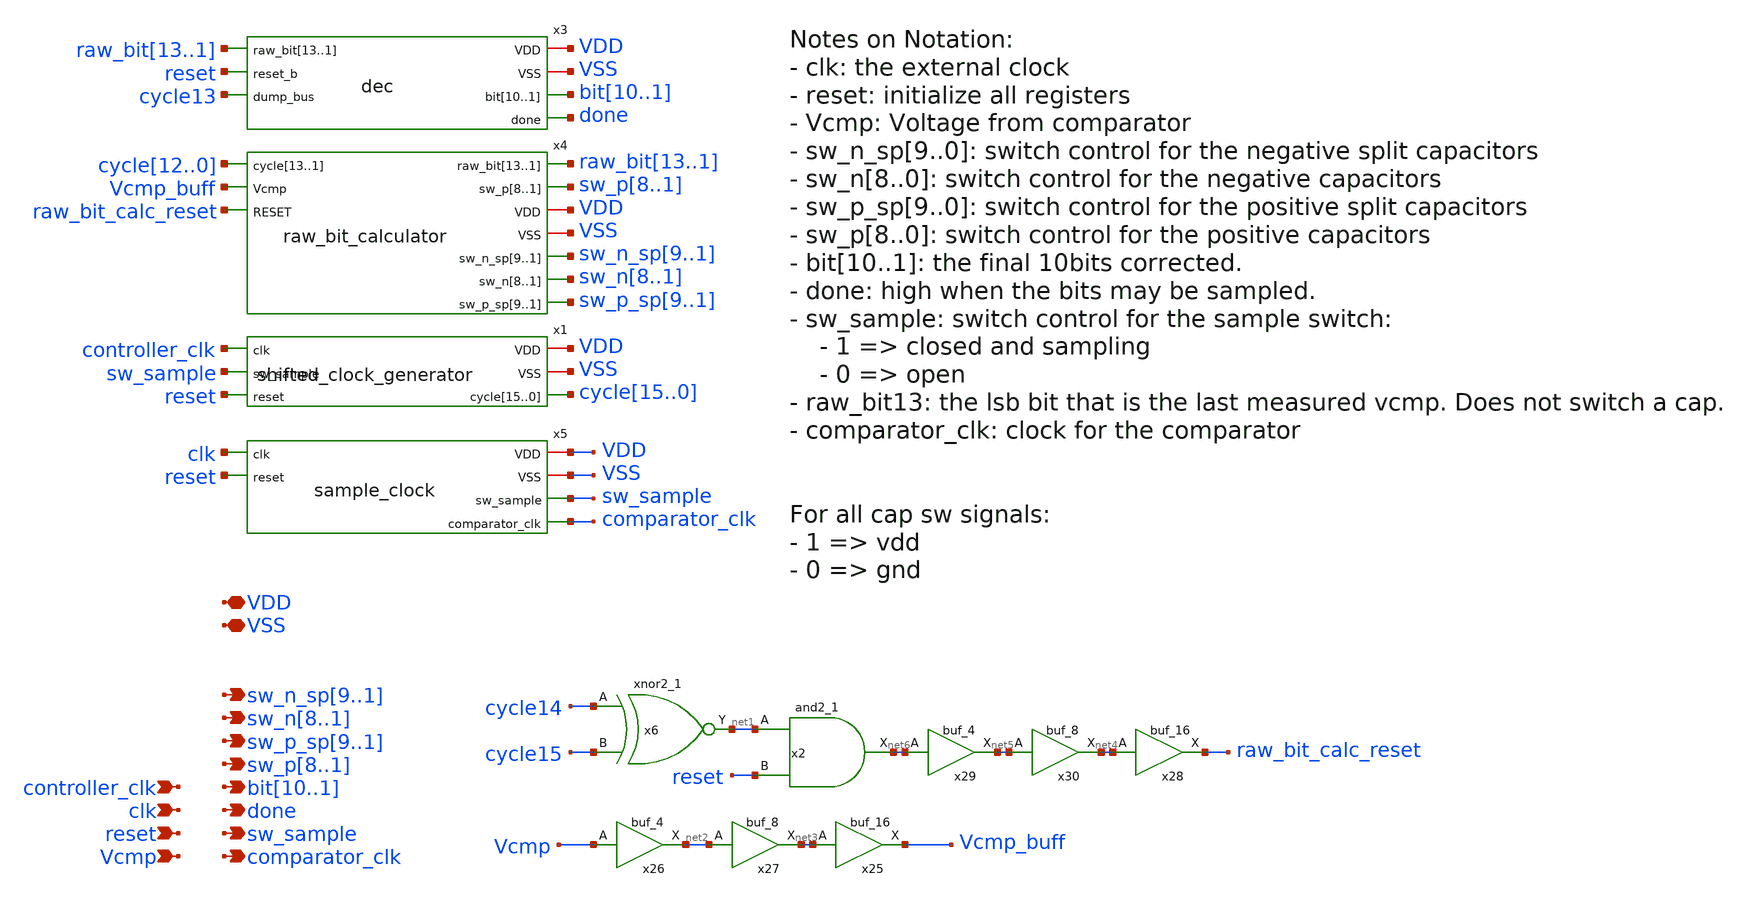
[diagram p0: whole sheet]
** sch_path: xschem/src/controller/controller.sch
**.subckt controller clk
*+ sw_n_sp9,sw_n_sp8,sw_n_sp7,sw_n_sp6,sw_n_sp5,sw_n_sp4,sw_n_sp3,sw_n_sp2,sw_n_sp1 VSS VDD reset Vcmp sw_n8,sw_n7,sw_n6,sw_n5,sw_n4,sw_n3,sw_n2,sw_n1
*+ sw_p_sp9,sw_p_sp8,sw_p_sp7,sw_p_sp6,sw_p_sp5,sw_p_sp4,sw_p_sp3,sw_p_sp2,sw_p_sp1 sw_p8,sw_p7,sw_p6,sw_p5,sw_p4,sw_p3,sw_p2,sw_p1 bit10,bit9,bit8,bit7,bit6,bit5,bit4,bit3,bit2,bit1
*+ done sw_sample controller_clk comparator_clk
*.ipin clk
*.opin sw_n_sp9,sw_n_sp8,sw_n_sp7,sw_n_sp6,sw_n_sp5,sw_n_sp4,sw_n_sp3,sw_n_sp2,sw_n_sp1
*.iopin VSS
*.iopin VDD
*.ipin reset
*.ipin Vcmp
*.opin sw_n8,sw_n7,sw_n6,sw_n5,sw_n4,sw_n3,sw_n2,sw_n1
*.opin sw_p_sp9,sw_p_sp8,sw_p_sp7,sw_p_sp6,sw_p_sp5,sw_p_sp4,sw_p_sp3,sw_p_sp2,sw_p_sp1
*.opin sw_p8,sw_p7,sw_p6,sw_p5,sw_p4,sw_p3,sw_p2,sw_p1
*.opin bit10,bit9,bit8,bit7,bit6,bit5,bit4,bit3,bit2,bit1
*.opin done
*.opin sw_sample
*.ipin controller_clk
*.opin comparator_clk
x3 VDD raw_bit13 raw_bit12 raw_bit11 raw_bit10 raw_bit9 raw_bit8 raw_bit7 raw_bit6 raw_bit5 raw_bit4
+ raw_bit3 raw_bit2 raw_bit1 VSS reset bit10 bit9 bit8 bit7 bit6 bit5 bit4 bit3 bit2 bit1 done cycle13 dec
x4 raw_bit13 raw_bit12 raw_bit11 raw_bit10 raw_bit9 raw_bit8 raw_bit7 raw_bit6 raw_bit5 raw_bit4
+ raw_bit3 raw_bit2 raw_bit1 cycle12 cycle11 cycle10 cycle9 cycle8 cycle7 cycle6 cycle5 cycle4 cycle3 cycle2
+ cycle1 cycle0 sw_p8 sw_p7 sw_p6 sw_p5 sw_p4 sw_p3 sw_p2 sw_p1 Vcmp_buff raw_bit_calc_reset VDD VSS
+ sw_n_sp9 sw_n_sp8 sw_n_sp7 sw_n_sp6 sw_n_sp5 sw_n_sp4 sw_n_sp3 sw_n_sp2 sw_n_sp1 sw_n8 sw_n7 sw_n6 sw_n5
+ sw_n4 sw_n3 sw_n2 sw_n1 sw_p_sp9 sw_p_sp8 sw_p_sp7 sw_p_sp6 sw_p_sp5 sw_p_sp4 sw_p_sp3 sw_p_sp2 sw_p_sp1
+ raw_bit_calculator
x1 VDD controller_clk sw_sample VSS reset cycle15 cycle14 cycle13 cycle12 cycle11 cycle10 cycle9
+ cycle8 cycle7 cycle6 cycle5 cycle4 cycle3 cycle2 cycle1 cycle0 shifted_clock_generator
x2 net1 reset VSS VSS VDD VDD net6 sky130_fd_sc_hd__and2_1
x6 cycle14 cycle15 VSS VSS VDD VDD net1 sky130_fd_sc_hd__xnor2_1
x25 net3 VSS VSS VDD VDD Vcmp_buff sky130_fd_sc_hd__buf_16
x26 Vcmp VSS VSS VDD VDD net2 sky130_fd_sc_hd__buf_4
x27 net2 VSS VSS VDD VDD net3 sky130_fd_sc_hd__buf_8
x28 net4 VSS VSS VDD VDD raw_bit_calc_reset sky130_fd_sc_hd__buf_16
x29 net6 VSS VSS VDD VDD net5 sky130_fd_sc_hd__buf_4
x30 net5 VSS VSS VDD VDD net4 sky130_fd_sc_hd__buf_8
x5 VDD clk reset VSS sw_sample comparator_clk sample_clock
**.ends

* expanding   symbol:  src/dec/dec.sym # of pins=7
** sym_path: xschem/src/dec/dec.sym
** sch_path: xschem/src/dec/dec.sch
.subckt dec VDD raw_bit13 raw_bit12 raw_bit11 raw_bit10 raw_bit9 raw_bit8 raw_bit7 raw_bit6 raw_bit5
+ raw_bit4 raw_bit3 raw_bit2 raw_bit1 VSS reset_b bit10 bit9 bit8 bit7 bit6 bit5 bit4 bit3 bit2 bit1 done
+ dump_bus
*.iopin VDD
*.opin bit10,bit9,bit8,bit7,bit6,bit5,bit4,bit3,bit2,bit1
*.iopin VSS
*.ipin reset_b
*.ipin dump_bus
*.opin done
*.ipin
*+ raw_bit13,raw_bit12,raw_bit11,raw_bit10,raw_bit9,raw_bit8,raw_bit7,raw_bit6,raw_bit5,raw_bit4,raw_bit3,raw_bit2,raw_bit1
x62 raw_bit2 raw_bit1 net1 VSS VSS VDD VDD net16 net2 sky130_fd_sc_hd__fa_1
x64 raw_bit3 raw_bit1 net4 VSS VSS VDD VDD net1 net3 sky130_fd_sc_hd__fa_1
x67 dump_bus net2 reset_b VSS VSS VDD VDD bit2 sky130_fd_sc_hd__dfrtp_1
x68 dump_bus net3 reset_b VSS VSS VDD VDD bit3 sky130_fd_sc_hd__dfrtp_1
x65 raw_bit5 raw_bit4 net5 VSS VSS VDD VDD net4 net6 sky130_fd_sc_hd__fa_1
x69 raw_bit6 raw_bit4 net8 VSS VSS VDD VDD net5 net7 sky130_fd_sc_hd__fa_1
x70 dump_bus net6 reset_b VSS VSS VDD VDD bit4 sky130_fd_sc_hd__dfrtp_1
x71 dump_bus net7 reset_b VSS VSS VDD VDD bit5 sky130_fd_sc_hd__dfrtp_1
x72 raw_bit7 raw_bit4 net9 VSS VSS VDD VDD net8 net10 sky130_fd_sc_hd__fa_1
x73 raw_bit9 raw_bit8 net12 VSS VSS VDD VDD net9 net11 sky130_fd_sc_hd__fa_1
x74 dump_bus net10 reset_b VSS VSS VDD VDD bit6 sky130_fd_sc_hd__dfrtp_1
x75 dump_bus net11 reset_b VSS VSS VDD VDD bit7 sky130_fd_sc_hd__dfrtp_1
x76 raw_bit10 raw_bit8 net13 VSS VSS VDD VDD net12 net14 sky130_fd_sc_hd__fa_1
x77 raw_bit11 raw_bit8 raw_bit12 VSS VSS VDD VDD net13 net15 sky130_fd_sc_hd__fa_1
x78 dump_bus net14 reset_b VSS VSS VDD VDD bit8 sky130_fd_sc_hd__dfrtp_1
x79 dump_bus net15 reset_b VSS VSS VDD VDD bit9 sky130_fd_sc_hd__dfrtp_1
x80 dump_bus net16 reset_b VSS VSS VDD VDD bit1 sky130_fd_sc_hd__dfrtp_1
x81 dump_bus raw_bit13 reset_b VSS VSS VDD VDD bit10 sky130_fd_sc_hd__dfrtp_1
x82 dump_bus VSS VSS VDD VDD done sky130_fd_sc_hd__inv_1
* noconn done
.ends


* expanding   symbol:  src/raw_bit_calculator/raw_bit_calculator.sym # of pins=10
** sym_path: xschem/src/raw_bit_calculator/raw_bit_calculator.sym
** sch_path: xschem/src/raw_bit_calculator/raw_bit_calculator.sch
.subckt raw_bit_calculator raw_bit13 raw_bit12 raw_bit11 raw_bit10 raw_bit9 raw_bit8 raw_bit7
+ raw_bit6 raw_bit5 raw_bit4 raw_bit3 raw_bit2 raw_bit1 cycle13 cycle12 cycle11 cycle10 cycle9 cycle8 cycle7
+ cycle6 cycle5 cycle4 cycle3 cycle2 cycle1 sw_p8 sw_p7 sw_p6 sw_p5 sw_p4 sw_p3 sw_p2 sw_p1 Vcmp RESET VDD
+ VSS sw_n_sp9 sw_n_sp8 sw_n_sp7 sw_n_sp6 sw_n_sp5 sw_n_sp4 sw_n_sp3 sw_n_sp2 sw_n_sp1 sw_n8 sw_n7 sw_n6
+ sw_n5 sw_n4 sw_n3 sw_n2 sw_n1 sw_p_sp9 sw_p_sp8 sw_p_sp7 sw_p_sp6 sw_p_sp5 sw_p_sp4 sw_p_sp3 sw_p_sp2
+ sw_p_sp1
*.ipin
*+ cycle13,cycle12,cycle11,cycle10,cycle9,cycle8,cycle7,cycle6,cycle5,cycle4,cycle3,cycle2,cycle1
*.opin sw_n_sp9,sw_n_sp8,sw_n_sp7,sw_n_sp6,sw_n_sp5,sw_n_sp4,sw_n_sp3,sw_n_sp2,sw_n_sp1
*.iopin VSS
*.iopin VDD
*.opin sw_n8,sw_n7,sw_n6,sw_n5,sw_n4,sw_n3,sw_n2,sw_n1
*.opin sw_p_sp9,sw_p_sp8,sw_p_sp7,sw_p_sp6,sw_p_sp5,sw_p_sp4,sw_p_sp3,sw_p_sp2,sw_p_sp1
*.opin sw_p8,sw_p7,sw_p6,sw_p5,sw_p4,sw_p3,sw_p2,sw_p1
*.ipin Vcmp
*.ipin RESET
*.opin
*+ raw_bit13,raw_bit12,raw_bit11,raw_bit10,raw_bit9,raw_bit8,raw_bit7,raw_bit6,raw_bit5,raw_bit4,raw_bit3,raw_bit2,raw_bit1
x29 raw_bit1 Vcmp VSS VSS VDD VDD net58 sky130_fd_sc_hd__xor2_1
x31 raw_bit1 Vcmp VSS VSS VDD VDD net62 sky130_fd_sc_hd__xor2_1
x37 raw_bit4 Vcmp VSS VSS VDD VDD net52 sky130_fd_sc_hd__xor2_1
x40 raw_bit4 Vcmp VSS VSS VDD VDD net53 sky130_fd_sc_hd__xor2_1
x45 raw_bit4 Vcmp VSS VSS VDD VDD net54 sky130_fd_sc_hd__xor2_1
x100 cycle1 net11 net23 VSS VSS VDD VDD sw_p_sp1 sky130_fd_sc_hd__dfrtp_1
x99 Vcmp VSS VSS VDD VDD net11 sky130_fd_sc_hd__inv_1
x102 cycle1 Vcmp net23 VSS VSS VDD VDD sw_n_sp1 sky130_fd_sc_hd__dfrtp_1
x25 cycle1 Vcmp net25 VSS VSS VDD VDD sw_n_sp2 sky130_fd_sc_hd__dfrtp_1
x103 Vcmp VSS VSS VDD VDD net12 sky130_fd_sc_hd__inv_1
x104 cycle1 net12 net25 VSS VSS VDD VDD sw_p_sp2 sky130_fd_sc_hd__dfrtp_1
x21 net1 Vcmp RESET VSS VSS VDD VDD sw_n1 sky130_fd_sc_hd__dfstp_1
x22 net1 net13 RESET VSS VSS VDD VDD sw_p1 sky130_fd_sc_hd__dfstp_1
x105 Vcmp VSS VSS VDD VDD net13 sky130_fd_sc_hd__inv_1
x28 net4 Vcmp RESET VSS VSS VDD VDD sw_n2 sky130_fd_sc_hd__dfstp_1
x106 net4 net14 RESET VSS VSS VDD VDD sw_p2 sky130_fd_sc_hd__dfstp_1
x107 Vcmp VSS VSS VDD VDD net14 sky130_fd_sc_hd__inv_1
x109 Vcmp VSS VSS VDD VDD net15 sky130_fd_sc_hd__inv_1
x111 Vcmp VSS VSS VDD VDD net16 sky130_fd_sc_hd__inv_1
x27 cycle4 Vcmp net27 VSS VSS VDD VDD sw_n_sp3 sky130_fd_sc_hd__dfrtp_1
x35 cycle4 net15 net27 VSS VSS VDD VDD sw_p_sp3 sky130_fd_sc_hd__dfrtp_1
x41 cycle4 Vcmp net28 VSS VSS VDD VDD sw_n_sp4 sky130_fd_sc_hd__dfrtp_1
x108 cycle4 net16 net28 VSS VSS VDD VDD sw_p_sp4 sky130_fd_sc_hd__dfrtp_1
x110 cycle4 Vcmp net29 VSS VSS VDD VDD sw_n_sp5 sky130_fd_sc_hd__dfrtp_1
x112 cycle4 net17 net29 VSS VSS VDD VDD sw_p_sp5 sky130_fd_sc_hd__dfrtp_1
x113 Vcmp VSS VSS VDD VDD net17 sky130_fd_sc_hd__inv_1
x114 net6 net18 RESET VSS VSS VDD VDD sw_p3 sky130_fd_sc_hd__dfstp_1
x32 net6 Vcmp RESET VSS VSS VDD VDD sw_n3 sky130_fd_sc_hd__dfstp_1
x115 Vcmp VSS VSS VDD VDD net18 sky130_fd_sc_hd__inv_1
x38 net7 Vcmp RESET VSS VSS VDD VDD sw_n4 sky130_fd_sc_hd__dfstp_1
x116 net7 net19 RESET VSS VSS VDD VDD sw_p4 sky130_fd_sc_hd__dfstp_1
x117 Vcmp VSS VSS VDD VDD net19 sky130_fd_sc_hd__inv_1
x43 net8 Vcmp RESET VSS VSS VDD VDD sw_n5 sky130_fd_sc_hd__dfstp_1
x118 net8 net20 RESET VSS VSS VDD VDD sw_p5 sky130_fd_sc_hd__dfstp_1
x119 Vcmp VSS VSS VDD VDD net20 sky130_fd_sc_hd__inv_1
x132 cycle12 net21 RESET VSS VSS VDD VDD sw_p_sp9 sky130_fd_sc_hd__dfrtp_1
x133 Vcmp VSS VSS VDD VDD net21 sky130_fd_sc_hd__inv_1
x61 cycle12 Vcmp RESET VSS VSS VDD VDD sw_n_sp9 sky130_fd_sc_hd__dfrtp_1
x24 net51 VDD VSS net1 net3 net2 demux2
x30 net61 VDD VSS net4 net60 net5 demux2
x34 net65 VDD VSS net6 net64 net22 demux2
x39 net68 VDD VSS net7 net67 net9 demux2
x44 net71 VDD VSS net8 net70 net10 demux2
x1 net2 VSS VSS VDD VDD net24 sky130_fd_sc_hd__inv_1
x2 net5 VSS VSS VDD VDD net26 sky130_fd_sc_hd__inv_1
x3 cycle1 Vcmp RESET VSS VSS VDD VDD raw_bit1 sky130_fd_sc_hd__dfrtp_4
x4 cycle2 Vcmp RESET VSS VSS VDD VDD raw_bit2 sky130_fd_sc_hd__dfrtp_4
x5 cycle3 Vcmp RESET VSS VSS VDD VDD raw_bit3 sky130_fd_sc_hd__dfrtp_4
x6 cycle4 Vcmp RESET VSS VSS VDD VDD raw_bit4 sky130_fd_sc_hd__dfrtp_4
x7 cycle5 Vcmp RESET VSS VSS VDD VDD raw_bit5 sky130_fd_sc_hd__dfrtp_4
x8 cycle6 Vcmp RESET VSS VSS VDD VDD raw_bit6 sky130_fd_sc_hd__dfrtp_4
x9 cycle7 Vcmp RESET VSS VSS VDD VDD raw_bit7 sky130_fd_sc_hd__dfrtp_4
x10 cycle8 Vcmp RESET VSS VSS VDD VDD raw_bit8 sky130_fd_sc_hd__dfrtp_4
x11 cycle9 Vcmp RESET VSS VSS VDD VDD raw_bit9 sky130_fd_sc_hd__dfrtp_4
x12 cycle10 Vcmp RESET VSS VSS VDD VDD raw_bit10 sky130_fd_sc_hd__dfrtp_4
x13 cycle11 Vcmp RESET VSS VSS VDD VDD raw_bit11 sky130_fd_sc_hd__dfrtp_4
x14 cycle12 Vcmp RESET VSS VSS VDD VDD raw_bit12 sky130_fd_sc_hd__dfrtp_4
x15 cycle13 Vcmp RESET VSS VSS VDD VDD raw_bit13 sky130_fd_sc_hd__dfrtp_4
x18 net22 VSS VSS VDD VDD net30 sky130_fd_sc_hd__inv_1
x19 net9 VSS VSS VDD VDD net31 sky130_fd_sc_hd__inv_1
x20 net10 VSS VSS VDD VDD net32 sky130_fd_sc_hd__inv_1
x42 raw_bit8 Vcmp VSS VSS VDD VDD net55 sky130_fd_sc_hd__xor2_1
x62 raw_bit8 Vcmp VSS VSS VDD VDD net56 sky130_fd_sc_hd__xor2_1
x64 raw_bit8 Vcmp VSS VSS VDD VDD net57 sky130_fd_sc_hd__xor2_1
x65 Vcmp VSS VSS VDD VDD net38 sky130_fd_sc_hd__inv_1
x66 Vcmp VSS VSS VDD VDD net39 sky130_fd_sc_hd__inv_1
x67 cycle8 Vcmp net45 VSS VSS VDD VDD sw_n_sp6 sky130_fd_sc_hd__dfrtp_1
x68 cycle8 net38 net45 VSS VSS VDD VDD sw_p_sp6 sky130_fd_sc_hd__dfrtp_1
x69 cycle8 Vcmp net46 VSS VSS VDD VDD sw_n_sp7 sky130_fd_sc_hd__dfrtp_1
x70 cycle8 net39 net46 VSS VSS VDD VDD sw_p_sp7 sky130_fd_sc_hd__dfrtp_1
x71 cycle8 Vcmp net47 VSS VSS VDD VDD sw_n_sp8 sky130_fd_sc_hd__dfrtp_1
x72 cycle8 net40 net47 VSS VSS VDD VDD sw_p_sp8 sky130_fd_sc_hd__dfrtp_1
x73 Vcmp VSS VSS VDD VDD net40 sky130_fd_sc_hd__inv_1
x74 net33 net41 RESET VSS VSS VDD VDD sw_p6 sky130_fd_sc_hd__dfstp_1
x75 net33 Vcmp RESET VSS VSS VDD VDD sw_n6 sky130_fd_sc_hd__dfstp_1
x76 Vcmp VSS VSS VDD VDD net41 sky130_fd_sc_hd__inv_1
x77 net34 Vcmp RESET VSS VSS VDD VDD sw_n7 sky130_fd_sc_hd__dfstp_1
x78 net34 net42 RESET VSS VSS VDD VDD sw_p7 sky130_fd_sc_hd__dfstp_1
x79 Vcmp VSS VSS VDD VDD net42 sky130_fd_sc_hd__inv_1
x80 net35 Vcmp RESET VSS VSS VDD VDD sw_n8 sky130_fd_sc_hd__dfstp_1
x81 net35 net43 RESET VSS VSS VDD VDD sw_p8 sky130_fd_sc_hd__dfstp_1
x82 Vcmp VSS VSS VDD VDD net43 sky130_fd_sc_hd__inv_1
x83 net74 VDD VSS net33 net73 net44 demux2
x84 net77 VDD VSS net34 net76 net36 demux2
x85 net80 VDD VSS net35 net79 net37 demux2
x88 net44 VSS VSS VDD VDD net48 sky130_fd_sc_hd__inv_1
x89 net36 VSS VSS VDD VDD net49 sky130_fd_sc_hd__inv_1
x90 net37 VSS VSS VDD VDD net50 sky130_fd_sc_hd__inv_1
x46 net24 RESET VSS VSS VDD VDD net23 sky130_fd_sc_hd__and2_0
x23 net26 RESET VSS VSS VDD VDD net25 sky130_fd_sc_hd__and2_0
x26 net30 RESET VSS VSS VDD VDD net27 sky130_fd_sc_hd__and2_0
x16 net31 RESET VSS VSS VDD VDD net28 sky130_fd_sc_hd__and2_0
x17 net32 RESET VSS VSS VDD VDD net29 sky130_fd_sc_hd__and2_0
x33 net48 RESET VSS VSS VDD VDD net45 sky130_fd_sc_hd__and2_0
x36 net49 RESET VSS VSS VDD VDD net46 sky130_fd_sc_hd__and2_0
x47 net50 RESET VSS VSS VDD VDD net47 sky130_fd_sc_hd__and2_0
x48 cycle2 net58 RESET VSS VSS VDD VDD net51 sky130_fd_sc_hd__dfrtp_1
x49 net59 VSS VSS VDD VDD net3 sky130_fd_sc_hd__clkdlybuf4s50_1
x50 cycle2 VSS VSS VDD VDD net59 sky130_fd_sc_hd__clkdlybuf4s50_1
x51 cycle3 net62 RESET VSS VSS VDD VDD net61 sky130_fd_sc_hd__dfrtp_1
x52 net63 VSS VSS VDD VDD net60 sky130_fd_sc_hd__clkdlybuf4s50_1
x53 cycle3 VSS VSS VDD VDD net63 sky130_fd_sc_hd__clkdlybuf4s50_1
x54 cycle5 net52 RESET VSS VSS VDD VDD net65 sky130_fd_sc_hd__dfrtp_1
x55 net66 VSS VSS VDD VDD net64 sky130_fd_sc_hd__clkdlybuf4s50_1
x56 cycle5 VSS VSS VDD VDD net66 sky130_fd_sc_hd__clkdlybuf4s50_1
x57 cycle6 net53 RESET VSS VSS VDD VDD net68 sky130_fd_sc_hd__dfrtp_1
x58 net69 VSS VSS VDD VDD net67 sky130_fd_sc_hd__clkdlybuf4s50_1
x59 cycle6 VSS VSS VDD VDD net69 sky130_fd_sc_hd__clkdlybuf4s50_1
x60 cycle7 net54 RESET VSS VSS VDD VDD net71 sky130_fd_sc_hd__dfrtp_1
x63 net72 VSS VSS VDD VDD net70 sky130_fd_sc_hd__clkdlybuf4s50_1
x86 cycle7 VSS VSS VDD VDD net72 sky130_fd_sc_hd__clkdlybuf4s50_1
x87 cycle9 net55 RESET VSS VSS VDD VDD net74 sky130_fd_sc_hd__dfrtp_1
x91 net75 VSS VSS VDD VDD net73 sky130_fd_sc_hd__clkdlybuf4s50_1
x92 cycle9 VSS VSS VDD VDD net75 sky130_fd_sc_hd__clkdlybuf4s50_1
x93 cycle10 net56 RESET VSS VSS VDD VDD net77 sky130_fd_sc_hd__dfrtp_1
x94 net78 VSS VSS VDD VDD net76 sky130_fd_sc_hd__clkdlybuf4s50_1
x95 cycle10 VSS VSS VDD VDD net78 sky130_fd_sc_hd__clkdlybuf4s50_1
x96 cycle11 net57 RESET VSS VSS VDD VDD net80 sky130_fd_sc_hd__dfrtp_1
x97 net81 VSS VSS VDD VDD net79 sky130_fd_sc_hd__clkdlybuf4s50_1
x98 cycle11 VSS VSS VDD VDD net81 sky130_fd_sc_hd__clkdlybuf4s50_1
.ends


* expanding   symbol:  src/shifted_clock_generator/shifted_clock_generator.sym # of pins=6
** sym_path: xschem/src/shifted_clock_generator/shifted_clock_generator.sym
** sch_path: xschem/src/shifted_clock_generator/shifted_clock_generator.sch
.subckt shifted_clock_generator VDD clk sw_sample VSS reset cycle15 cycle14 cycle13 cycle12 cycle11
+ cycle10 cycle9 cycle8 cycle7 cycle6 cycle5 cycle4 cycle3 cycle2 cycle1 cycle0
*.opin
*+ cycle15,cycle14,cycle13,cycle12,cycle11,cycle10,cycle9,cycle8,cycle7,cycle6,cycle5,cycle4,cycle3,cycle2,cycle1,cycle0
*.iopin VSS
*.iopin VDD
*.ipin clk
*.ipin reset
*.ipin sw_sample
x32 net16 net17 reset_b VSS VSS VDD VDD net4 sky130_fd_sc_hd__dfrtp_1
x1 net5 net4 reset_b VSS VSS VDD VDD net18 sky130_fd_sc_hd__dfrtp_1
x2 net6 net18 reset_b VSS VSS VDD VDD net19 sky130_fd_sc_hd__dfrtp_1
x3 net7 net19 reset_b VSS VSS VDD VDD net20 sky130_fd_sc_hd__dfrtp_1
x4 net8 net20 reset_b VSS VSS VDD VDD net21 sky130_fd_sc_hd__dfrtp_1
x5 net9 net21 reset_b VSS VSS VDD VDD net22 sky130_fd_sc_hd__dfrtp_1
x6 net10 net22 reset_b VSS VSS VDD VDD net23 sky130_fd_sc_hd__dfrtp_1
x7 net11 net23 reset_b VSS VSS VDD VDD net24 sky130_fd_sc_hd__dfrtp_1
x8 net12 net24 reset_b VSS VSS VDD VDD net25 sky130_fd_sc_hd__dfrtp_1
x9 net13 net25 reset_b VSS VSS VDD VDD net26 sky130_fd_sc_hd__dfrtp_1
x10 net14 net26 reset_b VSS VSS VDD VDD net27 sky130_fd_sc_hd__dfrtp_1
x11 net15 net27 reset_b VSS VSS VDD VDD net28 sky130_fd_sc_hd__dfrtp_1
x12 net3 net28 reset_b VSS VSS VDD VDD net29 sky130_fd_sc_hd__dfrtp_1
x13 net1 net29 reset_b VSS VSS VDD VDD net30 sky130_fd_sc_hd__dfrtp_1
x14 net2 net30 reset_b VSS VSS VDD VDD net31 sky130_fd_sc_hd__dfrtp_1
x31 net32 net33 reset_b VSS VSS VDD VDD net17 sky130_fd_sc_hd__dfrtp_1
x37 net35 VSS VSS VDD VDD reset_b sky130_fd_sc_hd__buf_16
x35 net34 reset VSS VSS VDD VDD net35 sky130_fd_sc_hd__and2_4
x15 net17 VSS VSS VDD VDD net46 sky130_fd_sc_hd__buf_1
x16 net44 VSS VSS VDD VDD net36 sky130_fd_sc_hd__buf_2
x20 net44 VSS VSS VDD VDD net37 sky130_fd_sc_hd__buf_2
x21 net44 VSS VSS VDD VDD net38 sky130_fd_sc_hd__buf_2
x22 net44 VSS VSS VDD VDD net39 sky130_fd_sc_hd__buf_2
x23 net45 VSS VSS VDD VDD net40 sky130_fd_sc_hd__buf_2
x24 net45 VSS VSS VDD VDD net41 sky130_fd_sc_hd__buf_2
x25 net45 VSS VSS VDD VDD net42 sky130_fd_sc_hd__buf_2
x26 net45 VSS VSS VDD VDD net43 sky130_fd_sc_hd__buf_2
x27 clk VSS VSS VDD VDD net44 sky130_fd_sc_hd__buf_4
x28 clk VSS VSS VDD VDD net45 sky130_fd_sc_hd__buf_4
x17 net36 VSS VSS VDD VDD net32 sky130_fd_sc_hd__buf_1
x18 net36 VSS VSS VDD VDD net16 sky130_fd_sc_hd__buf_1
x19 net37 VSS VSS VDD VDD net5 sky130_fd_sc_hd__buf_1
x29 net37 VSS VSS VDD VDD net6 sky130_fd_sc_hd__buf_1
x30 net38 VSS VSS VDD VDD net7 sky130_fd_sc_hd__buf_1
x33 net38 VSS VSS VDD VDD net8 sky130_fd_sc_hd__buf_1
x47 net39 VSS VSS VDD VDD net9 sky130_fd_sc_hd__buf_1
x48 net39 VSS VSS VDD VDD net10 sky130_fd_sc_hd__buf_1
x51 net40 VSS VSS VDD VDD net11 sky130_fd_sc_hd__buf_1
x52 net40 VSS VSS VDD VDD net12 sky130_fd_sc_hd__buf_1
x53 net41 VSS VSS VDD VDD net13 sky130_fd_sc_hd__buf_1
x54 net41 VSS VSS VDD VDD net14 sky130_fd_sc_hd__buf_1
x55 net42 VSS VSS VDD VDD net15 sky130_fd_sc_hd__buf_1
x56 net42 VSS VSS VDD VDD net3 sky130_fd_sc_hd__buf_1
x57 net43 VSS VSS VDD VDD net1 sky130_fd_sc_hd__buf_1
x58 net43 VSS VSS VDD VDD net2 sky130_fd_sc_hd__buf_1
x62 net4 VSS VSS VDD VDD net47 sky130_fd_sc_hd__buf_1
x66 net18 VSS VSS VDD VDD net48 sky130_fd_sc_hd__buf_1
x70 net19 VSS VSS VDD VDD net49 sky130_fd_sc_hd__buf_1
x34 sw_sample VSS VSS VDD VDD net34 sky130_fd_sc_hd__inv_1
x36 VDD VSS VSS VDD VDD net33 sky130_fd_sc_hd__buf_1
x38 net46 VSS VSS VDD VDD cycle0 sky130_fd_sc_hd__buf_4
x39 net47 VSS VSS VDD VDD cycle1 sky130_fd_sc_hd__buf_4
x40 net48 VSS VSS VDD VDD cycle2 sky130_fd_sc_hd__buf_4
x41 net49 VSS VSS VDD VDD cycle3 sky130_fd_sc_hd__buf_4
x42 net20 VSS VSS VDD VDD net50 sky130_fd_sc_hd__buf_1
x43 net21 VSS VSS VDD VDD net51 sky130_fd_sc_hd__buf_1
x44 net22 VSS VSS VDD VDD net52 sky130_fd_sc_hd__buf_1
x45 net23 VSS VSS VDD VDD net53 sky130_fd_sc_hd__buf_1
x46 net50 VSS VSS VDD VDD cycle4 sky130_fd_sc_hd__buf_4
x49 net51 VSS VSS VDD VDD cycle5 sky130_fd_sc_hd__buf_4
x50 net52 VSS VSS VDD VDD cycle6 sky130_fd_sc_hd__buf_4
x59 net53 VSS VSS VDD VDD cycle7 sky130_fd_sc_hd__buf_4
x60 net24 VSS VSS VDD VDD net54 sky130_fd_sc_hd__buf_1
x61 net25 VSS VSS VDD VDD net55 sky130_fd_sc_hd__buf_1
x63 net26 VSS VSS VDD VDD net56 sky130_fd_sc_hd__buf_1
x64 net27 VSS VSS VDD VDD net57 sky130_fd_sc_hd__buf_1
x65 net54 VSS VSS VDD VDD cycle8 sky130_fd_sc_hd__buf_4
x67 net55 VSS VSS VDD VDD cycle9 sky130_fd_sc_hd__buf_4
x68 net56 VSS VSS VDD VDD cycle10 sky130_fd_sc_hd__buf_4
x69 net57 VSS VSS VDD VDD cycle11 sky130_fd_sc_hd__buf_4
x71 net28 VSS VSS VDD VDD net58 sky130_fd_sc_hd__buf_1
x72 net29 VSS VSS VDD VDD net59 sky130_fd_sc_hd__buf_1
x73 net30 VSS VSS VDD VDD net60 sky130_fd_sc_hd__buf_1
x74 net31 VSS VSS VDD VDD net61 sky130_fd_sc_hd__buf_1
x75 net58 VSS VSS VDD VDD cycle12 sky130_fd_sc_hd__buf_4
x76 net59 VSS VSS VDD VDD cycle13 sky130_fd_sc_hd__buf_4
x77 net60 VSS VSS VDD VDD cycle14 sky130_fd_sc_hd__buf_4
x78 net61 VSS VSS VDD VDD cycle15 sky130_fd_sc_hd__buf_4
.ends


* expanding   symbol:  src/sample_clock/sample_clock.sym # of pins=6
** sym_path: xschem/src/sample_clock/sample_clock.sym
** sch_path: xschem/src/sample_clock/sample_clock.sch
.subckt sample_clock VDD clk reset VSS sw_sample comparator_clk
*.iopin VDD
*.ipin clk
*.opin sw_sample
*.iopin VSS
*.opin comparator_clk
*.ipin reset
x5 clk johnson_counter_loop reset VSS VSS VDD VDD sw_sample sky130_fd_sc_hd__dfrtp_1
x7 clk sw_sample reset VSS VSS VDD VDD net1 sky130_fd_sc_hd__dfrtp_1
x8 clk net1 reset VSS VSS VDD VDD net2 sky130_fd_sc_hd__dfrtp_1
x9 clk net2 reset VSS VSS VDD VDD net3 sky130_fd_sc_hd__dfrtp_1
x10 clk net3 reset VSS VSS VDD VDD net4 sky130_fd_sc_hd__dfrtp_1
x11 clk net4 reset VSS VSS VDD VDD net5 sky130_fd_sc_hd__dfrtp_1
x12 clk net5 reset VSS VSS VDD VDD net6 sky130_fd_sc_hd__dfrtp_1
x13 clk net6 reset VSS VSS VDD VDD net7 sky130_fd_sc_hd__dfrtp_1
x14 clk net7 reset VSS VSS VDD VDD net8 sky130_fd_sc_hd__dfrtp_1
x15 clk net8 reset VSS VSS VDD VDD net9 sky130_fd_sc_hd__dfrtp_1
x16 clk net9 reset VSS VSS VDD VDD net10 sky130_fd_sc_hd__dfrtp_1
x17 clk net10 reset VSS VSS VDD VDD net11 sky130_fd_sc_hd__dfrtp_1
x18 clk net11 reset VSS VSS VDD VDD net12 sky130_fd_sc_hd__dfrtp_1
x19 clk net12 reset VSS VSS VDD VDD net13 sky130_fd_sc_hd__dfrtp_1
x20 clk net13 reset VSS VSS VDD VDD net14 sky130_fd_sc_hd__dfrtp_1
x21 clk net14 reset VSS VSS VDD VDD net15 sky130_fd_sc_hd__dfrtp_1
x22 net15 VSS VSS VDD VDD johnson_counter_loop sky130_fd_sc_hd__inv_1
x23 clk net16 VSS VSS VDD VDD net19 sky130_fd_sc_hd__and2_1
x24 sw_sample VSS VSS VDD VDD net16 sky130_fd_sc_hd__inv_1
x25 net18 VSS VSS VDD VDD comparator_clk sky130_fd_sc_hd__buf_16
x26 net20 VSS VSS VDD VDD net17 sky130_fd_sc_hd__buf_4
x27 net17 VSS VSS VDD VDD net18 sky130_fd_sc_hd__buf_8
x1 net19 VSS VSS VDD VDD net20 sky130_fd_sc_hd__buf_2
.ends


* expanding   symbol:  src/demux2/demux2.sym # of pins=6
** sym_path: xschem/src/demux2/demux2.sym
** sch_path: xschem/src/demux2/demux2.sch
.subckt demux2 S VDD VSS OUT_0 IN OUT_1
*.ipin S
*.opin OUT_0
*.ipin IN
*.opin OUT_1
*.iopin VDD
*.iopin VSS
x1 net1 IN VSS VSS VDD VDD OUT_0 sky130_fd_sc_hd__and2_0
x2 S IN VSS VSS VDD VDD OUT_1 sky130_fd_sc_hd__and2_0
x3 S VSS VSS VDD VDD net1 sky130_fd_sc_hd__inv_1
.ends

.end
